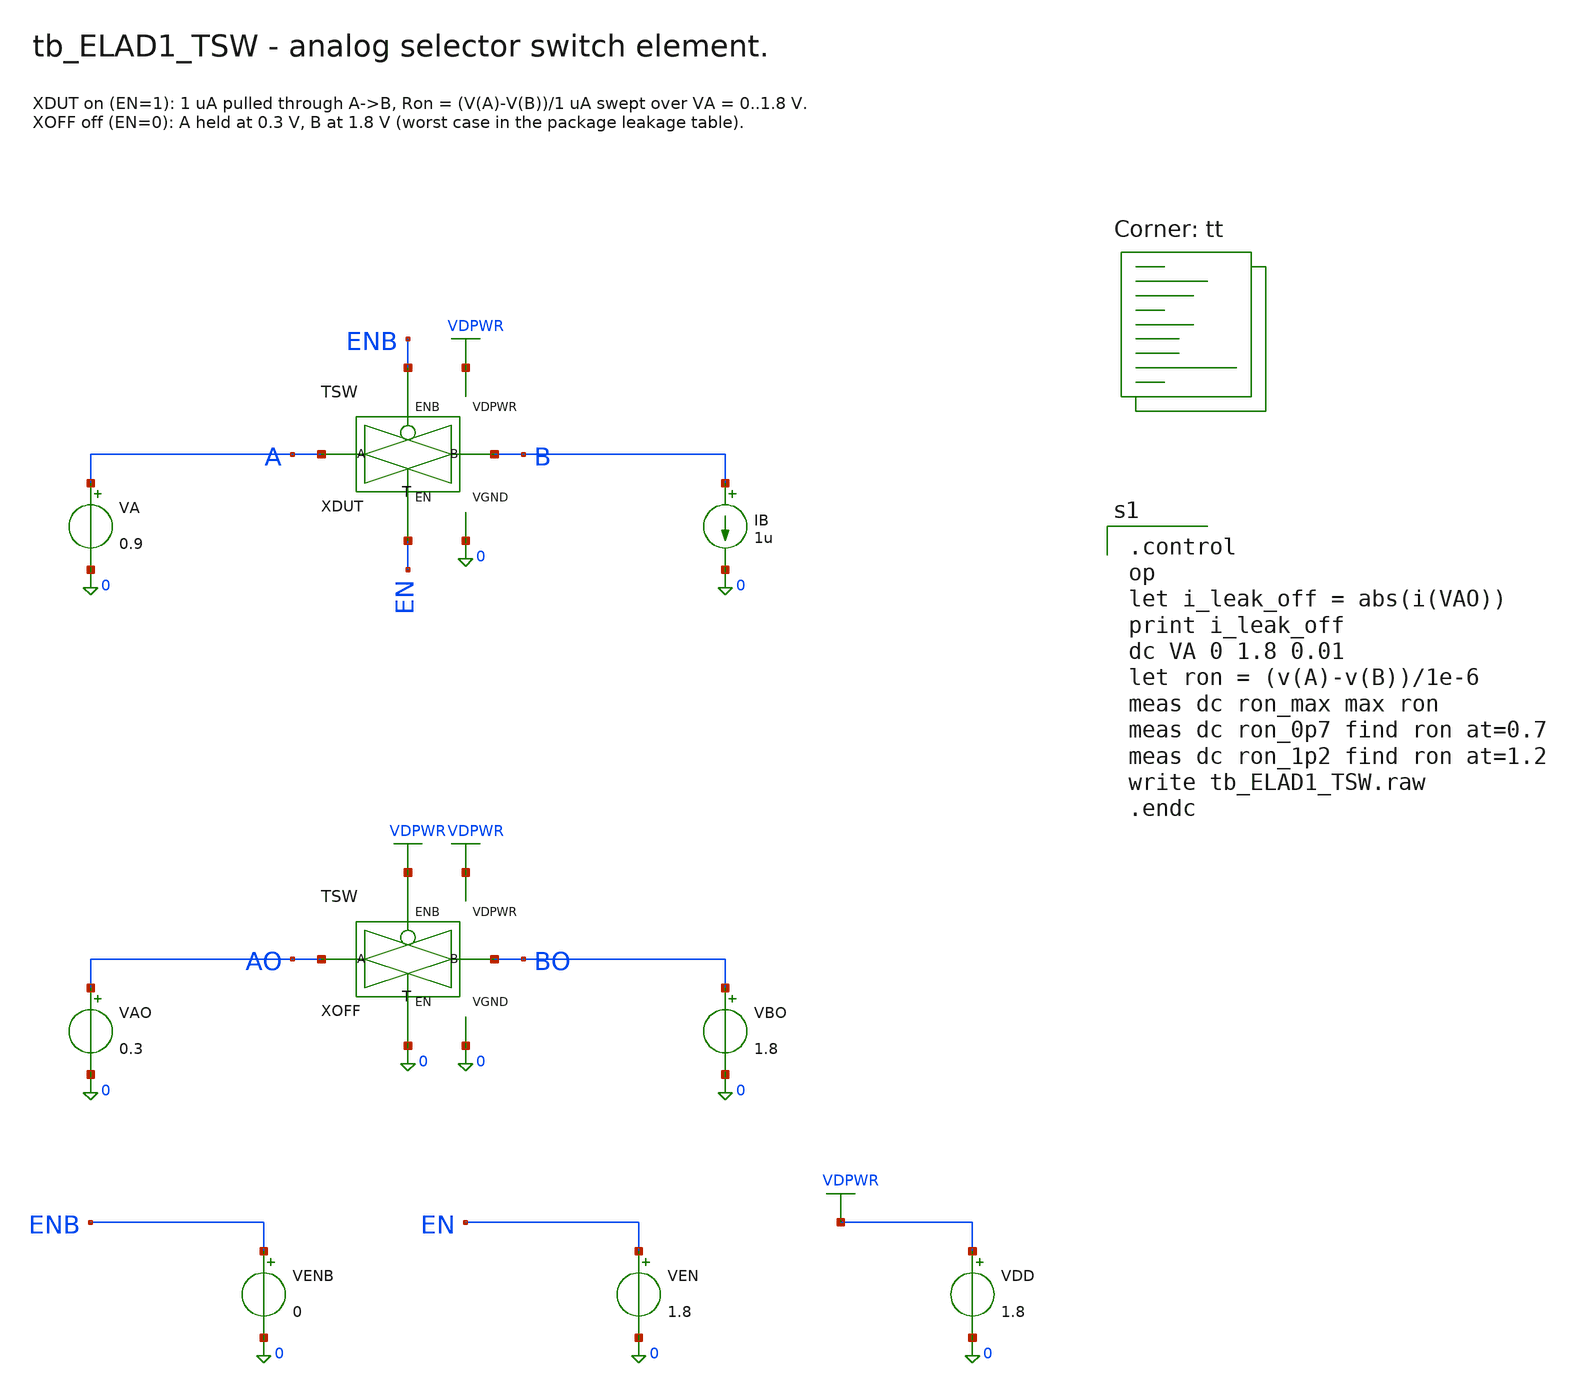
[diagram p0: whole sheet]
** sch_path: cells/ELAD1_TSW/schematic/tb_ELAD1_TSW.sch
**.subckt tb_ELAD1_TSW
XDUT A B EN ENB VDPWR 0 ELAD1_TSW
VA A 0 0.9
IB B 0 1u
XOFF AO BO 0 VDPWR VDPWR 0 ELAD1_TSW
VAO AO 0 0.3
VBO BO 0 1.8
VENB ENB 0 0
VEN EN 0 1.8
VDD VDPWR 0 1.8
**** begin user architecture code

.control
op
let i_leak_off = abs(i(VAO))
print i_leak_off
dc VA 0 1.8 0.01
let ron = (v(A)-v(B))/1e-6
meas dc ron_max max ron
meas dc ron_0p7 find ron at=0.7
meas dc ron_1p2 find ron at=1.2
write tb_ELAD1_TSW.raw
.endc

.lib $::SKYWATER_MODELS/sky130.lib.spice tt
**** end user architecture code
**.ends

* expanding   symbol:  ELAD1_TSW.sym # of pins=6
** sym_path: cells/ELAD1_TSW/schematic/ELAD1_TSW.sym
** sch_path: cells/ELAD1_TSW/schematic/ELAD1_TSW.sch
.subckt ELAD1_TSW A B EN ENB VDPWR VGND
*.iopin A
*.iopin B
*.iopin EN
*.iopin ENB
*.iopin VDPWR
*.iopin VGND
X1 A M EN ENB VDPWR VGND ELAD1_TGA
X2 M B EN ENB VDPWR VGND ELAD1_TGA
XSH M ENB VGND VGND sky130_fd_pr__nfet_01v8 L=0.15 W=1 nf=1 ad='int((1 + 1)/2) * 1 / 1 * 0.29' as='int((1 + 2)/2) * 1 / 1 * 0.29'
+ pd='2*int((1 + 1)/2) * (1 / 1 + 0.29)' ps='2*int((1 + 2)/2) * (1 / 1 + 0.29)' nrd='0.29 / 1 ' nrs='0.29 / 1 '
+ sa=0 sb=0 sd=0 mult=1 m=1
.ends


* expanding   symbol:  ELAD1_TGA.sym # of pins=6
** sym_path: cells/ELAD1_TGA/schematic/ELAD1_TGA.sym
** sch_path: cells/ELAD1_TGA/schematic/ELAD1_TGA.sch
.subckt ELAD1_TGA A B EN ENB VDPWR VGND
*.iopin A
*.iopin B
*.iopin EN
*.iopin ENB
*.iopin VDPWR
*.iopin VGND
XMN A EN B VGND sky130_fd_pr__nfet_01v8_lvt L=0.15 W=4 nf=1 ad='int((1 + 1)/2) * 4 / 1 * 0.29' as='int((1 + 2)/2) * 4 / 1 * 0.29'
+ pd='2*int((1 + 1)/2) * (4 / 1 + 0.29)' ps='2*int((1 + 2)/2) * (4 / 1 + 0.29)' nrd='0.29 / 4 ' nrs='0.29 / 4 '
+ sa=0 sb=0 sd=0 mult=1 m=1
XMP A ENB B VDPWR sky130_fd_pr__pfet_01v8_lvt L=0.35 W=12 nf=1 ad='int((1 + 1)/2) * 12 / 1 * 0.29' as='int((1 + 2)/2) * 12 / 1 * 0.29'
+ pd='2*int((1 + 1)/2) * (12 / 1 + 0.29)' ps='2*int((1 + 2)/2) * (12 / 1 + 0.29)' nrd='0.29 / 12 ' nrs='0.29 / 12 '
+ sa=0 sb=0 sd=0 mult=1 m=1
.ends

.end
